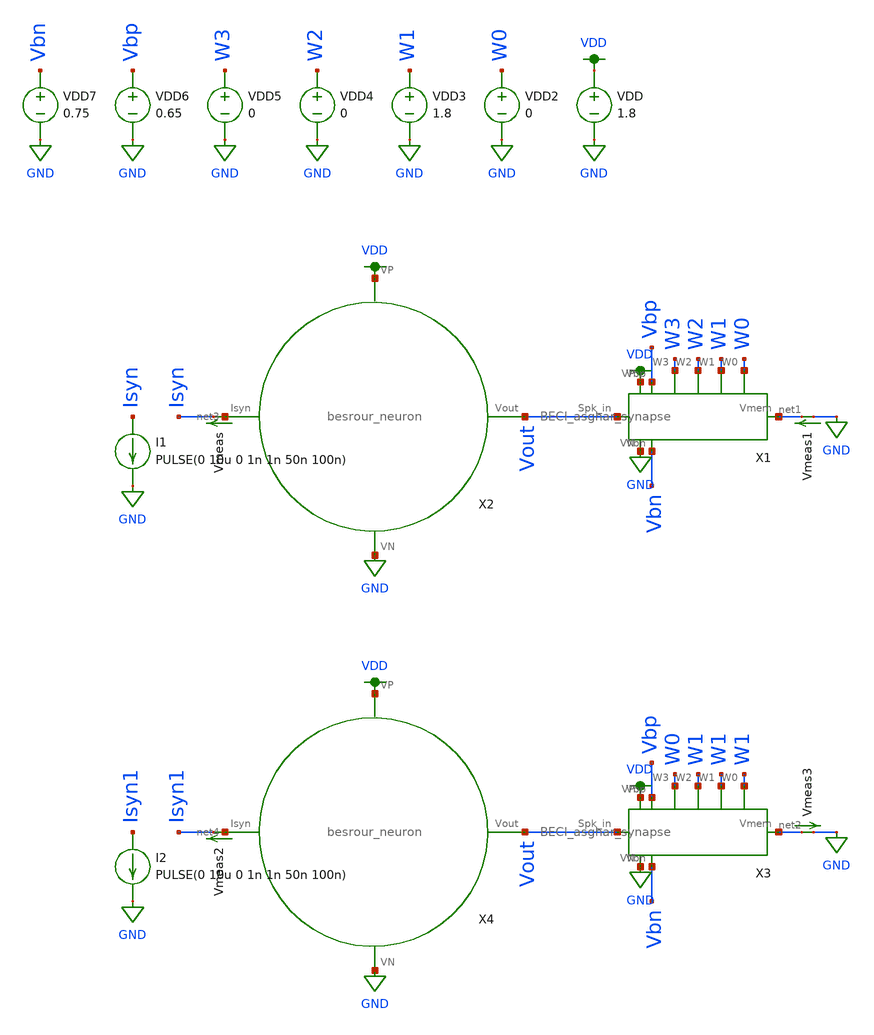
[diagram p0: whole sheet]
** sch_path: schematic/tran_neuron.sch
**.subckt tran_neuron
VDD VDD GND 1.8
I1 Isyn GND PULSE(0 10u 0 1n 1n 50n 100n)
Vmeas net3 Isyn 0
.save i(vmeas)
VDD2 W0 GND 0
VDD3 W1 GND 1.8
VDD4 W2 GND 0
VDD5 W3 GND 0
VDD6 Vbp GND 0.65
VDD7 Vbn GND 0.75
Vmeas1 GND net1 0
.save i(vmeas1)
X1 VDD GND Vout net1 W3 W2 W1 W0 Vbp Vbn BECI_asghar_synapse
X2 net3 Vout VDD GND besrour_neuron
I2 Isyn1 GND PULSE(0 10u 0 1n 1n 50n 100n)
Vmeas2 net4 Isyn1 0
.save i(vmeas2)
Vmeas3 net2 GND 0
.save i(vmeas3)
X3 VDD GND Vout net2 W0 W1 W1 W1 Vbp Vbn BECI_asghar_synapse
X4 net4 Vout VDD GND besrour_neuron
**** begin user architecture code

.param W=12
.param L=0.5
.tran 0.1n 250n
.save all


.option wnflag=1
.param MC_SWITCH=0.0
.lib ~/skywater/skywater-pdk/libraries/sky130_fd_pr_ngspice/latest/models/sky130.lib.spice tt

**** end user architecture code
**.ends
.GLOBAL GND
.GLOBAL VDD
.end
